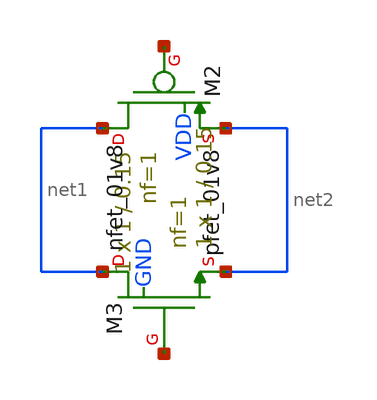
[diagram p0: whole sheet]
** sch_path: blocks/02_CMFB/xschem/TG.sch
**.subckt TG
XM2 net1 net3 net2 VDD sky130_fd_pr__pfet_01v8 L=0.15 W=1 nf=1 ad='int((1 + 1)/2) * 1 / 1 * 0.29' as='int((1 + 2)/2) * 1 / 1 * 0.29'
+ pd='2*int((1 + 1)/2) * (1 / 1 + 0.29)' ps='2*int((1 + 2)/2) * (1 / 1 + 0.29)' nrd='0.29 / 1 ' nrs='0.29 / 1 '
+ sa=0 sb=0 sd=0 mult=1 m=1
XM3 net1 net4 net2 GND sky130_fd_pr__nfet_01v8 L=0.15 W=1 nf=1 ad='int((1 + 1)/2) * 1 / 1 * 0.29' as='int((1 + 2)/2) * 1 / 1 * 0.29'
+ pd='2*int((1 + 1)/2) * (1 / 1 + 0.29)' ps='2*int((1 + 2)/2) * (1 / 1 + 0.29)' nrd='0.29 / 1 ' nrs='0.29 / 1 '
+ sa=0 sb=0 sd=0 mult=1 m=1
**.ends
.end
